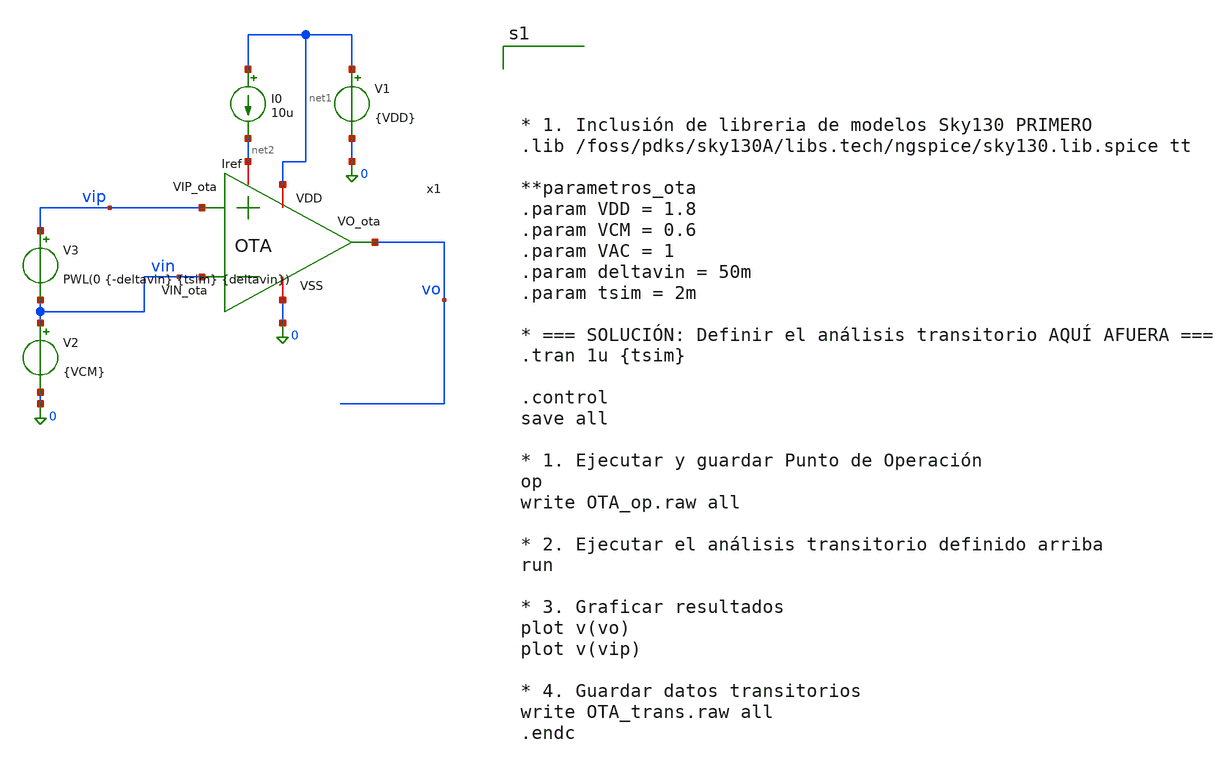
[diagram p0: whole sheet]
** sch_path: xschem/OTA_tbtran.sch
**.subckt OTA_tbtran
x1 net1 vo vin vip net2 0 OTA
V1 net1 0 {VDD}
I0 net1 net2 10u
V2 vin 0 {VCM}
V3 vip vin PWL(0 {-deltavin} {tsim} {deltavin})
**** begin user architecture code




* 1. Inclusión de libreria de modelos Sky130 PRIMERO
.lib /foss/pdks/sky130A/libs.tech/ngspice/sky130.lib.spice tt

**parametros_ota
.param VDD = 1.8
.param VCM = 0.6
.param VAC = 1
.param deltavin = 50m
.param tsim = 2m

* === SOLUCIÓN: Definir el análisis transitorio AQUÍ AFUERA ===
.tran 1u {tsim}

.control
save all

* 1. Ejecutar y guardar Punto de Operación
op
write OTA_op.raw all

* 2. Ejecutar el análisis transitorio definido arriba
run

* 3. Graficar resultados
plot v(vo)
plot v(vip)

* 4. Guardar datos transitorios
write OTA_trans.raw all
.endc



**** end user architecture code
**.ends

* expanding   symbol:  /foss/designs/LDO-sky130/xschem/OTA.sym # of pins=6
** sym_path: xschem/OTA.sym
** sch_path: xschem/OTA.sch
.subckt OTA VDD VO_ota VIN_ota VIP_ota Iref VSS
*.ipin VIN_ota
*.opin VO_ota
*.iopin Iref
*.iopin VSS
*.iopin VDD
*.ipin VIP_ota
XR1 VO_ota1 net1 VDD sky130_fd_pr__res_high_po W=0.35 L=360 mult=1 m=1
XC1 VO_ota net1 sky130_fd_pr__cap_mim_m3_2 W=50 L=50 MF=1 m=1
XMpr VO_ota1 net2 VSS VSS sky130_fd_pr__nfet_01v8 L=0.5 W=3 nf=1 ad='int((1 + 1)/2) * 3 / 1 * 0.29' as='int((1 + 2)/2) * 3 / 1 * 0.29'
+ pd='2*int((1 + 1)/2) * (3 / 1 + 0.29)' ps='2*int((1 + 2)/2) * (3 / 1 + 0.29)' nrd='0.29 / 3 ' nrs='0.29 / 3 '
+ sa=0 sb=0 sd=0 mult=1 m=1
XMnr net2 net2 VSS VSS sky130_fd_pr__nfet_01v8 L=0.5 W=3 nf=1 ad='int((1 + 1)/2) * 3 / 1 * 0.29' as='int((1 + 2)/2) * 3 / 1 * 0.29'
+ pd='2*int((1 + 1)/2) * (3 / 1 + 0.29)' ps='2*int((1 + 2)/2) * (3 / 1 + 0.29)' nrd='0.29 / 3 ' nrs='0.29 / 3 '
+ sa=0 sb=0 sd=0 mult=1 m=1
XMn net2 VIN_ota Vtail VDD sky130_fd_pr__pfet_01v8 L=0.5 W=28 nf=1 ad='int((1 + 1)/2) * 28 / 1 * 0.29'
+ as='int((1 + 2)/2) * 28 / 1 * 0.29' pd='2*int((1 + 1)/2) * (28 / 1 + 0.29)' ps='2*int((1 + 2)/2) * (28 / 1 + 0.29)'
+ nrd='0.29 / 28 ' nrs='0.29 / 28 ' sa=0 sb=0 sd=0 mult=1 m=1
XMp VO_ota1 VIP_ota Vtail VDD sky130_fd_pr__pfet_01v8 L=0.5 W=28 nf=1 ad='int((1 + 1)/2) * 28 / 1 * 0.29'
+ as='int((1 + 2)/2) * 28 / 1 * 0.29' pd='2*int((1 + 1)/2) * (28 / 1 + 0.29)' ps='2*int((1 + 2)/2) * (28 / 1 + 0.29)'
+ nrd='0.29 / 28 ' nrs='0.29 / 28 ' sa=0 sb=0 sd=0 mult=1 m=1
XMo VO_ota VO_ota1 VSS VSS sky130_fd_pr__nfet_01v8 L=0.5 W=3 nf=1 ad='int((1 + 1)/2) * 3 / 1 * 0.29'
+ as='int((1 + 2)/2) * 3 / 1 * 0.29' pd='2*int((1 + 1)/2) * (3 / 1 + 0.29)' ps='2*int((1 + 2)/2) * (3 / 1 + 0.29)'
+ nrd='0.29 / 3 ' nrs='0.29 / 3 ' sa=0 sb=0 sd=0 mult=1 m=1
XMc3 VGP Iref VSS VSS sky130_fd_pr__nfet_01v8 L=0.5 W=1 nf=1 ad='int((1 + 1)/2) * 1 / 1 * 0.29' as='int((1 + 2)/2) * 1 / 1 * 0.29'
+ pd='2*int((1 + 1)/2) * (1 / 1 + 0.29)' ps='2*int((1 + 2)/2) * (1 / 1 + 0.29)' nrd='0.29 / 1 ' nrs='0.29 / 1 '
+ sa=0 sb=0 sd=0 mult=1 m=1
XMp2 Iref Iref VSS VSS sky130_fd_pr__nfet_01v8 L=0.5 W=1 nf=1 ad='int((1 + 1)/2) * 1 / 1 * 0.29' as='int((1 + 2)/2) * 1 / 1 * 0.29'
+ pd='2*int((1 + 1)/2) * (1 / 1 + 0.29)' ps='2*int((1 + 2)/2) * (1 / 1 + 0.29)' nrd='0.29 / 1 ' nrs='0.29 / 1 '
+ sa=0 sb=0 sd=0 mult=1 m=1
XMr VGP VGP VDD VDD sky130_fd_pr__pfet_01v8_lvt L=0.5 W=2.4 nf=1 ad='int((1 + 1)/2) * 2.4 / 1 * 0.29'
+ as='int((1 + 2)/2) * 2.4 / 1 * 0.29' pd='2*int((1 + 1)/2) * (2.4 / 1 + 0.29)' ps='2*int((1 + 2)/2) * (2.4 / 1 + 0.29)'
+ nrd='0.29 / 2.4 ' nrs='0.29 / 2.4 ' sa=0 sb=0 sd=0 mult=1 m=1
XMrc1 Vtail VGP VDD VDD sky130_fd_pr__pfet_01v8_lvt L=0.5 W=19.4 nf=1 ad='int((1 + 1)/2) * 19.4 / 1 * 0.29'
+ as='int((1 + 2)/2) * 19.4 / 1 * 0.29' pd='2*int((1 + 1)/2) * (19.4 / 1 + 0.29)' ps='2*int((1 + 2)/2) * (19.4 / 1 + 0.29)'
+ nrd='0.29 / 19.4 ' nrs='0.29 / 19.4 ' sa=0 sb=0 sd=0 mult=1 m=1
XMrc2 VO_ota VGP VDD VDD sky130_fd_pr__pfet_01v8_lvt L=0.5 W=8 nf=1 ad='int((1 + 1)/2) * 8 / 1 * 0.29'
+ as='int((1 + 2)/2) * 8 / 1 * 0.29' pd='2*int((1 + 1)/2) * (8 / 1 + 0.29)' ps='2*int((1 + 2)/2) * (8 / 1 + 0.29)'
+ nrd='0.29 / 8 ' nrs='0.29 / 8 ' sa=0 sb=0 sd=0 mult=1 m=1
.ends

.end
